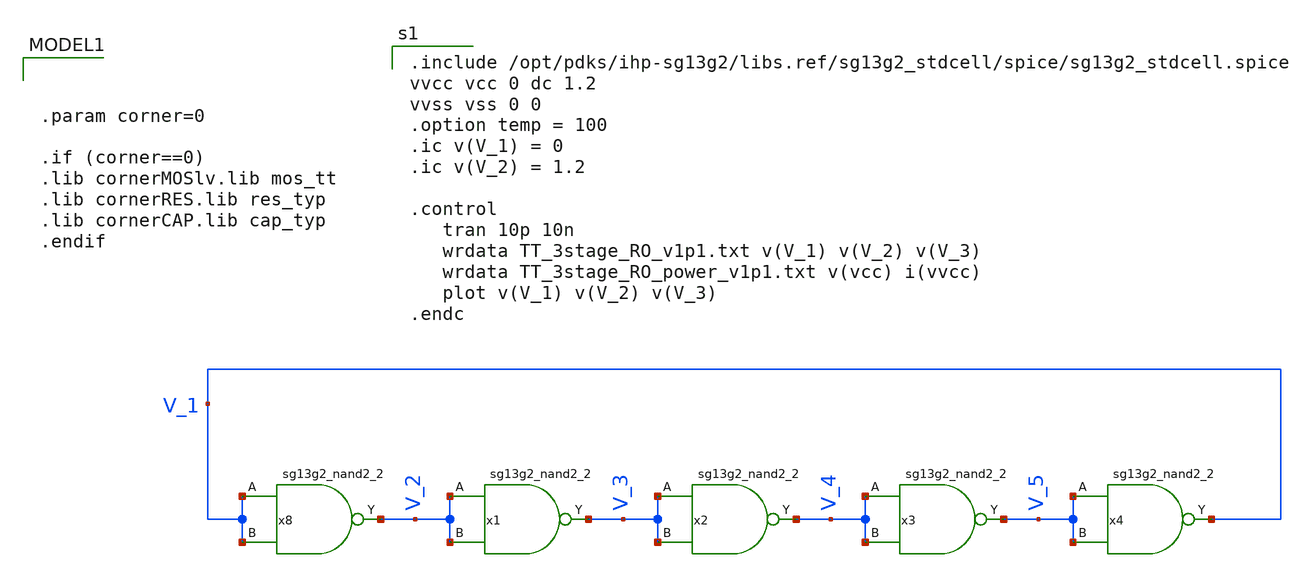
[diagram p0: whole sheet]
** sch_path: Day1/tb_7stage_dly_RO.sch
**.subckt tb_7stage_dly_RO
x8 V_2 V_1 V_1 VCC VSS sg13g2_nand2_2
x1 V_3 V_2 V_2 VCC VSS sg13g2_nand2_2
x2 V_4 V_3 V_3 VCC VSS sg13g2_nand2_2
x3 V_5 V_4 V_4 VCC VSS sg13g2_nand2_2
x4 V_1 V_5 V_5 VCC VSS sg13g2_nand2_2
**** begin user architecture code

.include /opt/pdks/ihp-sg13g2/libs.ref/sg13g2_stdcell/spice/sg13g2_stdcell.spice
vvcc vcc 0 dc 1.2
vvss vss 0 0
.option temp = 100
.ic v(V_1) = 0
.ic v(V_2) = 1.2

.control
   tran 10p 10n
   wrdata TT_3stage_RO_v1p1.txt v(V_1) v(V_2) v(V_3)
   wrdata TT_3stage_RO_power_v1p1.txt v(vcc) i(vvcc)
   plot v(V_1) v(V_2) v(V_3)
.endc




.param corner=0

.if (corner==0)
.lib cornerMOSlv.lib mos_tt
.lib cornerRES.lib res_typ
.lib cornerCAP.lib cap_typ
.endif

**** end user architecture code
**.ends

* expanding   symbol:  sg13g2_nand2_2.sym # of pins=3
** sym_path: sg13g2_nand2_2.sym
** sch_path: sg13g2_nand2_2.sch
.subckt sg13g2_nand2_2 Y A B VDD VSS
*.iopin VDD
*.iopin VSS
*.opin Y
*.ipin B
*.ipin A
XM1 Y A net1 VSS sg13_lv_nmos w=1.44u l=130.00n ng=2 m=1 mm_ok=1
XM2 net1 B VSS VSS sg13_lv_nmos w=1.44u l=130.00n ng=2 m=1 mm_ok=1
XM3 Y A VDD VDD sg13_lv_pmos w=2.24u l=130.00n ng=2 m=1 mm_ok=1
XM4 Y B VDD VDD sg13_lv_pmos w=2.24u l=130.00n ng=2 m=1 mm_ok=1
.ends

.end
